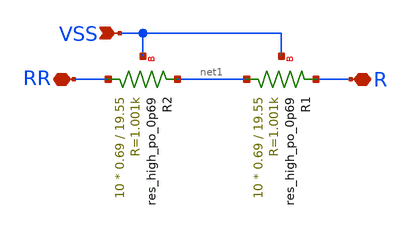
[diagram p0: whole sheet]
** sch_path: Res_2K.sch
**.subckt Res_2K R RR VSS
*.iopin R
*.iopin RR
*.ipin VSS
XR2 RR net1 VSS sky130_fd_pr__res_high_po_0p69 L=19.55 mult=10 m=10
XR1 net1 R VSS sky130_fd_pr__res_high_po_0p69 L=19.55 mult=10 m=10
**.ends
.end
